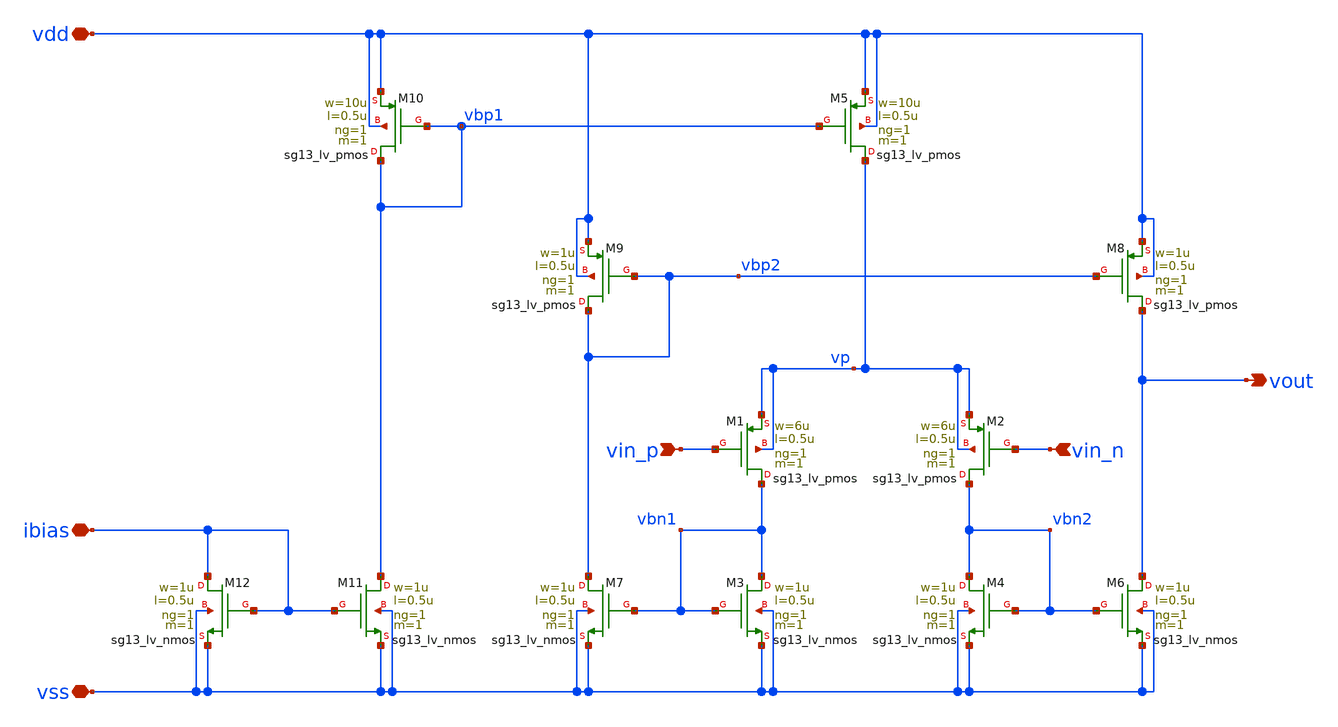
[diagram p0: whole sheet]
** sch_path: SSDOR_1.2V_v2/components/cgenerator/ota_cmp2.sch
**.subckt ota_cmp2 vdd vss ibias vin_p vin_n vout
*.iopin vdd
*.iopin vss
*.iopin ibias
*.ipin vin_p
*.ipin vin_n
*.opin vout
XM1 vbn1 vin_p vp vp sg13_lv_pmos w=6u l=0.5u ng=1 m=1 mm_ok=1
XM2 vbn2 vin_n vp vp sg13_lv_pmos w=6u l=0.5u ng=1 m=1 mm_ok=1
XM5 vp vbp1 vdd vdd sg13_lv_pmos w=10u l=0.5u ng=1 m=1 mm_ok=1
XM3 vbn1 vbn1 vss vss sg13_lv_nmos w=1u l=0.5u ng=1 m=1 mm_ok=1
XM4 vbn2 vbn2 vss vss sg13_lv_nmos w=1u l=0.5u ng=1 m=1 mm_ok=1
XM6 vout vbn2 vss vss sg13_lv_nmos w=1u l=0.5u ng=1 m=1 mm_ok=1
XM7 vbp2 vbn1 vss vss sg13_lv_nmos w=1u l=0.5u ng=1 m=1 mm_ok=1
XM8 vout vbp2 vdd vdd sg13_lv_pmos w=1u l=0.5u ng=1 m=1 mm_ok=1
XM9 vbp2 vbp2 vdd vdd sg13_lv_pmos w=1u l=0.5u ng=1 m=1 mm_ok=1
XM10 vbp1 vbp1 vdd vdd sg13_lv_pmos w=10u l=0.5u ng=1 m=1 mm_ok=1
XM11 vbp1 ibias vss vss sg13_lv_nmos w=1u l=0.5u ng=1 m=1 mm_ok=1
XM12 ibias ibias vss vss sg13_lv_nmos w=1u l=0.5u ng=1 m=1 mm_ok=1
**.ends
.end
